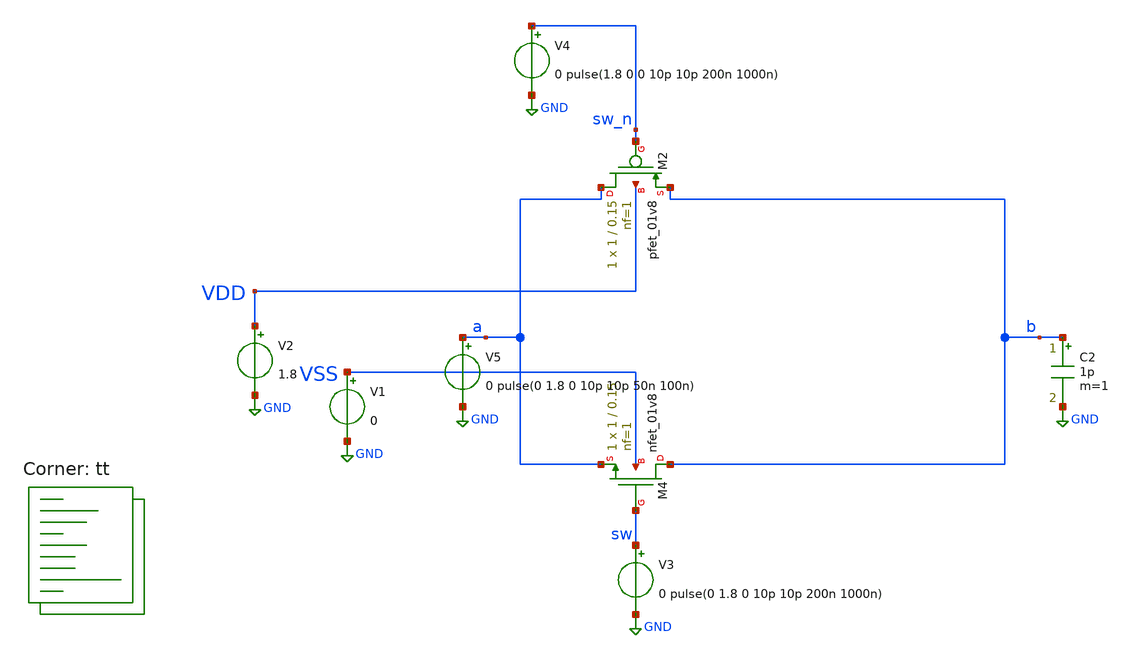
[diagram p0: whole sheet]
** sch_path: module/tah/tah2.sch
**.subckt tah2
XM4 b sw a VSS sky130_fd_pr__nfet_01v8 L=0.15 W=1 nf=1 ad='int((nf+1)/2) * W/nf * 0.29' as='int((nf+2)/2) * W/nf * 0.29'
+ pd='2*int((nf+1)/2) * (W/nf + 0.29)' ps='2*int((nf+2)/2) * (W/nf + 0.29)' nrd='0.29 / W' nrs='0.29 / W'
+ sa=0 sb=0 sd=0 mult=1 m=1
XM2 a sw_n b VDD sky130_fd_pr__pfet_01v8 L=0.15 W=1 nf=1 ad='int((nf+1)/2) * W/nf * 0.29' as='int((nf+2)/2) * W/nf * 0.29'
+ pd='2*int((nf+1)/2) * (W/nf + 0.29)' ps='2*int((nf+2)/2) * (W/nf + 0.29)' nrd='0.29 / W' nrs='0.29 / W'
+ sa=0 sb=0 sd=0 mult=1 m=1
V1 VSS GND 0
V2 VDD GND 1.8
V5 a GND 0 pulse(0 1.8 0 10p 10p 50n 100n)
C2 b GND 1p m=1
V3 sw GND 0 pulse(0 1.8 0 10p 10p 200n 1000n)
V4 sw_n GND 0 pulse(1.8 0 0 10p 10p 200n 1000n)
**** begin user architecture code


.save all
.temp = 25
.tran 100p 3000n
.OPTIONS savecurrents

.control
run
plot v(sw) v(sw_n) a b
plot in out
.endc


.lib $::SKYWATER_MODELS/sky130.lib.spice tt
**** end user architecture code
**.ends
.GLOBAL GND
.end
